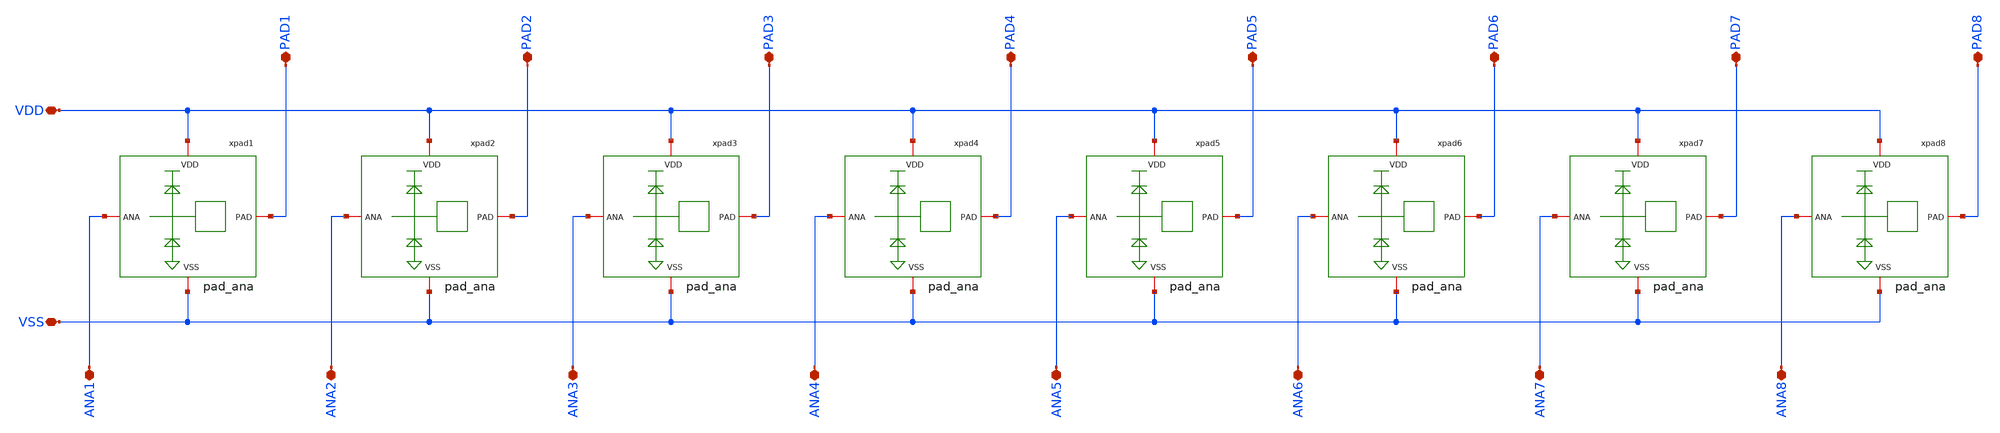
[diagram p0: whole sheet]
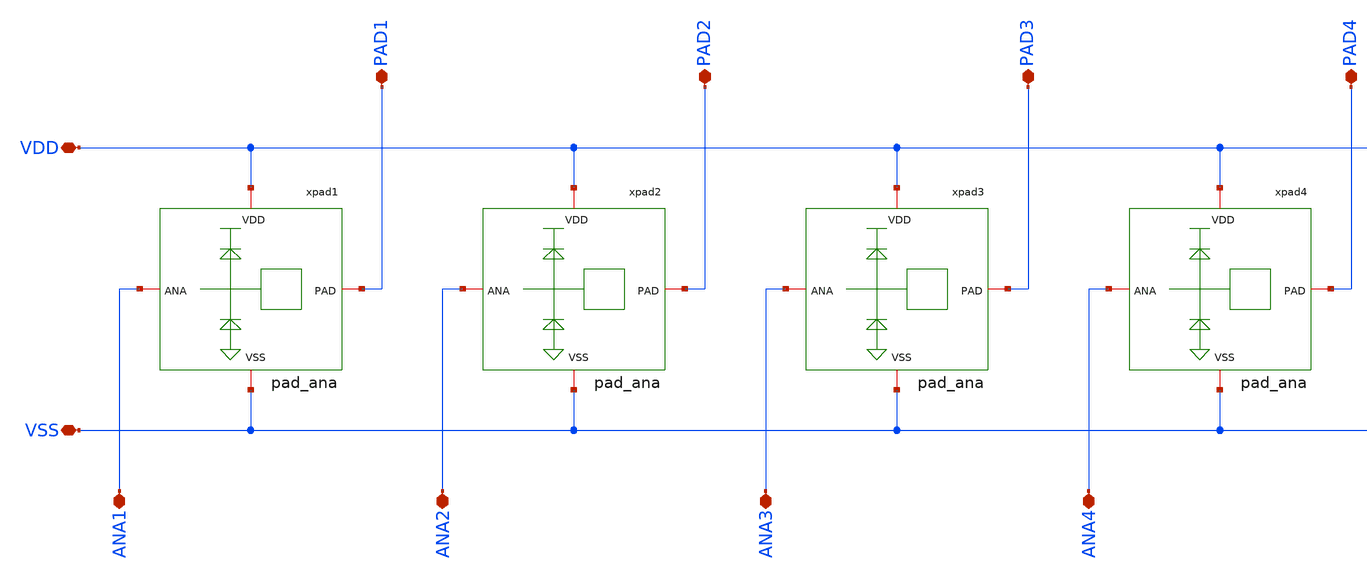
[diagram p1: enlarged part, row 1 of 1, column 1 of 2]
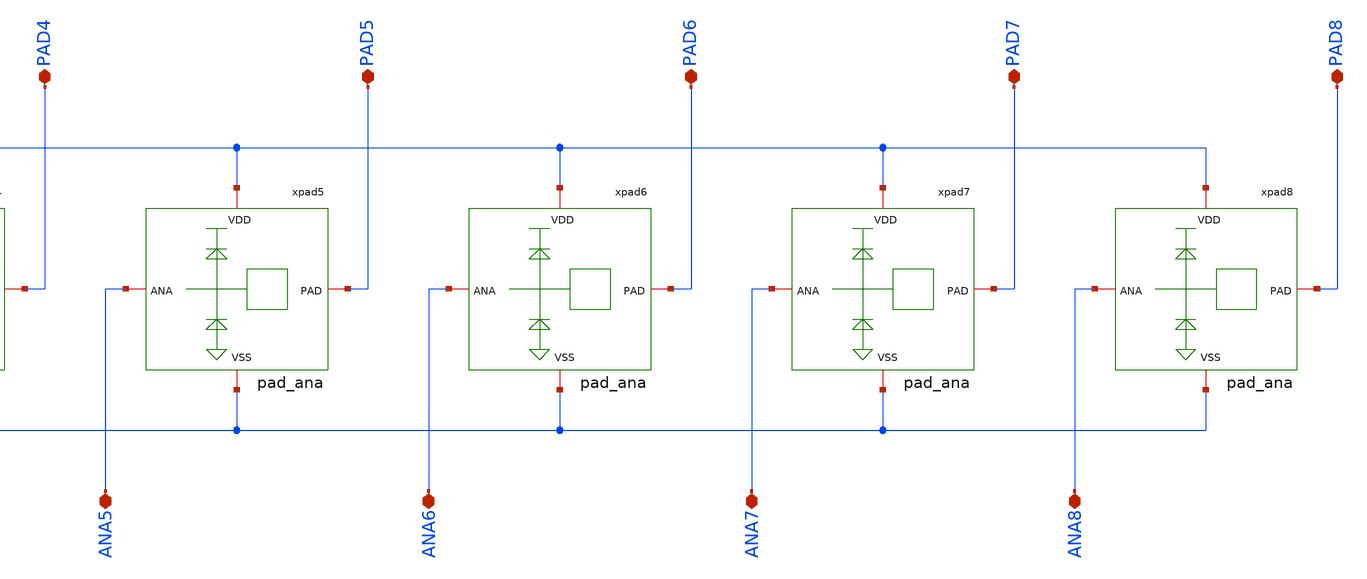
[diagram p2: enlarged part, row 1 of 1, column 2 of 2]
** sch_path: JKU_TC1/design_data/xschem/pads/pad_ana_x8.sch
**.subckt pad_ana_x8 VDD VSS ANA1 ANA2 ANA3 ANA4 ANA5 ANA6 ANA7 ANA8 PAD1 PAD2 PAD3 PAD4 PAD5 PAD6
*+ PAD7 PAD8
*.iopin VDD
*.iopin VSS
*.iopin ANA1
*.iopin ANA2
*.iopin ANA3
*.iopin ANA4
*.iopin ANA5
*.iopin ANA6
*.iopin ANA7
*.iopin ANA8
*.iopin PAD1
*.iopin PAD2
*.iopin PAD3
*.iopin PAD4
*.iopin PAD5
*.iopin PAD6
*.iopin PAD7
*.iopin PAD8
xpad1 VDD PAD1 ANA1 VSS pad_ana
xpad2 VDD PAD2 ANA2 VSS pad_ana
xpad3 VDD PAD3 ANA3 VSS pad_ana
xpad4 VDD PAD4 ANA4 VSS pad_ana
xpad5 VDD PAD5 ANA5 VSS pad_ana
xpad6 VDD PAD6 ANA6 VSS pad_ana
xpad7 VDD PAD7 ANA7 VSS pad_ana
xpad8 VDD PAD8 ANA8 VSS pad_ana
**.ends

* expanding   symbol:  pads/pad_ana.sym # of pins=4
** sym_path: JKU_TC1/design_data/xschem/pads/pad_ana.sym
** sch_path: JKU_TC1/design_data/xschem/pads/pad_ana.sch
.subckt pad_ana VDD PAD ANA VSS
*.iopin VSS
*.iopin PAD
*.iopin VDD
*.iopin ANA
XC1 VDD PAD cparasitic C=20f
XC2 PAD VSS cparasitic C=20f
R1 PAD ANA 1e-6 m=1
R2 PAD ANA 1e-6 m=1
xesd1 VDD PAD VSS pad_diodes
.ends


* expanding   symbol:  pads/pad_diodes.sym # of pins=3
** sym_path: JKU_TC1/design_data/xschem/pads/pad_diodes.sym
** sch_path: JKU_TC1/design_data/xschem/pads/pad_diodes.sch
.subckt pad_diodes VDD PAD VSS
*.iopin VDD
*.iopin VSS
*.iopin PAD
XXD1 PAD VDD dantenna l=780n w=780n
XXD2 VSS PAD dantenna l=780n w=780n
.ends

.end
